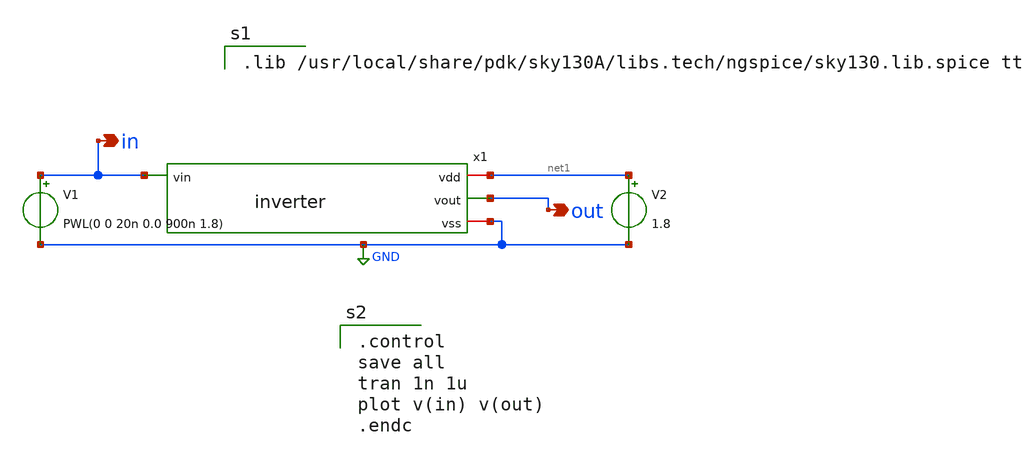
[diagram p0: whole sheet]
** sch_path: Lab1_inverter/xschem/inverter_tb.sch
**.subckt inverter_tb in out
*.opin in
*.opin out
V1 in GND PWL(0 0 20n 0.0 900n 1.8)
V2 net1 GND 1.8
x1 net1 in out GND inverter
**** begin user architecture code

.lib /usr/local/share/pdk/sky130A/libs.tech/ngspice/sky130.lib.spice tt


.control
save all
tran 1n 1u
plot v(in) v(out)
.endc

**** end user architecture code
**.ends

* expanding   symbol:  inverter.sym # of pins=4
** sym_path: Lab1_inverter/xschem/inverter.sym
** sch_path: Lab1_inverter/xschem/inverter.sch
.subckt inverter vdd vin vout vss
*.ipin vin
*.iopin vss
*.iopin vdd
*.opin vout
XM1 vout vin vss vss sky130_fd_pr__nfet_01v8 L=0.18 W=4.5 nf=3 ad='int((nf+1)/2) * W/nf * 0.29' as='int((nf+2)/2) * W/nf * 0.29'
+ pd='2*int((nf+1)/2) * (W/nf + 0.29)' ps='2*int((nf+2)/2) * (W/nf + 0.29)' nrd='0.29 / W' nrs='0.29 / W'
+ sa=0 sb=0 sd=0 mult=1 m=1
XM2 vout vin vdd vdd sky130_fd_pr__pfet_01v8 L=0.18 W=3 nf=3 ad='int((nf+1)/2) * W/nf * 0.29' as='int((nf+2)/2) * W/nf * 0.29'
+ pd='2*int((nf+1)/2) * (W/nf + 0.29)' ps='2*int((nf+2)/2) * (W/nf + 0.29)' nrd='0.29 / W' nrs='0.29 / W'
+ sa=0 sb=0 sd=0 mult=1 m=1
.ends

.GLOBAL GND
.end
